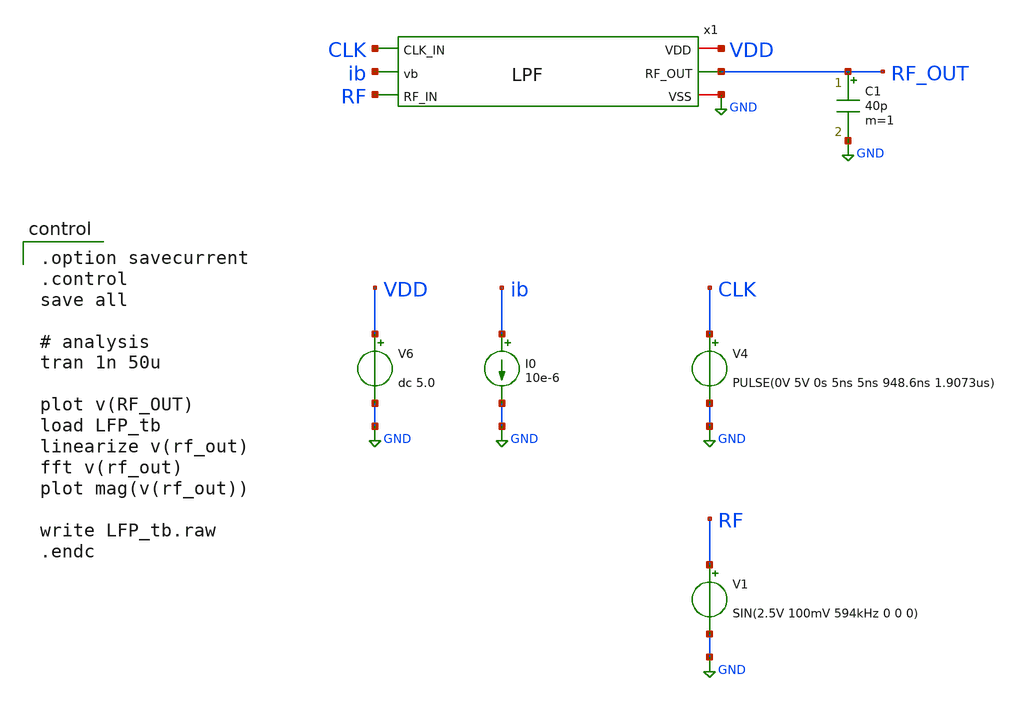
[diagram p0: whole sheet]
** sch_path: member_project/LPF/noritsuna/xschem/LPF_tb.sch
**.subckt LPF_tb
I0 ib GND 10e-6
V6 VDD GND dc 5.0
x1 CLK VDD GND ib RF_OUT RF LPF
C1 RF_OUT GND 40p m=1
V4 CLK GND PULSE(0V 5V 0s 5ns 5ns 948.6ns 1.9073us)
V1 RF GND SIN(2.5V 100mV 594kHz 0 0 0)
**** begin user architecture code
 .include $::LIB/ip62_models

.option savecurrent
.control
save all

# analysis
tran 1n 50u

plot v(RF_OUT)
load LFP_tb
linearize v(rf_out)
fft v(rf_out)
plot mag(v(rf_out))

write LFP_tb.raw
.endc

**** end user architecture code
**.ends
.GLOBAL GND
.end
